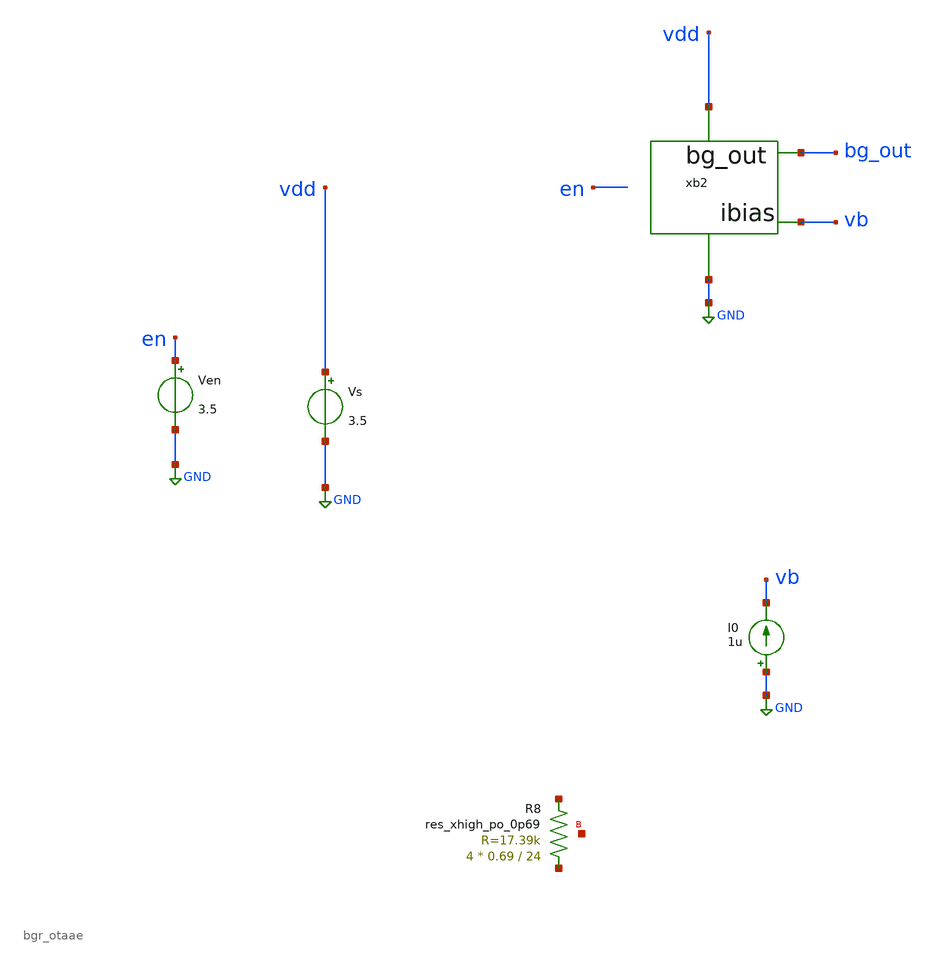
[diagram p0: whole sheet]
** sch_path: bg_sim_jm_otaam.sch
**.subckt bg_sim_jm_otaam
Vs vdd GND 3.5
Ven en GND 3.5
XR8 net1 net2 net3 sky130_fd_pr__res_xhigh_po_0p69 L=24 mult=4 m=4
I0 GND vb 1u
xb2 bg_out vb GND vdd bgr_otaae
**** begin user architecture code



.options method=gear
*.options method=trap
.options maxorder=3
.param R=36k
.save all
*R10 ldo_out GND {R}
*IL ldo_out 0 PWL(0 0.1m 10u 0.1m 20u 10m 30u 10m)
*CL ldo_out gnd 10p
*.lib /home/mustafa/mabrains/pdks/share/pdk/sky130A/libs.tech/ngspice/sky130.lib_mod.spice tt
.lib /foss/pdks/sky130A/libs.tech/ngspice/sky130.lib.spice TT





.nodeset v(x1.inn)=1.2
.nodeset v(x1.inp)=1.2
.nodeset v(x1.mir)=1
.nodeset v(x1.net5)=1
.nodeset v(x1.bg_out)=1.1
*.nodeset v(ldo_out)=1.8
*.nodeset v(pos)=1.1
*.nodeset v(net3)=0.8
*.nodeset v(net1)=0.7
.nodeset v(x1.net6)=0.9
*.nodeset v(net7)=0.75
.nodeset v(xy1.vb)=0.9


.option temp=27
*User_defined_functions
.control
define max(vector_name) (vecmax(vector_name))
define min(vector_name) (vecmin(vector_name))
.endc


*Temp_sweep
.control
*alter IL 0
dc temp 85 0 -1
let temp_coeff=1000000*(max(bg_out)-min(bg_out))/85
print temp_coeff
*plot v(ldo_out)
plot v(bg_out)
plot i(vs)
set wr_singlescale
set wr_vecnames
set appendwrite
.endc


.control
*alter IL 0
*alter R10 1G
op
let iq =i(Vs)
print iq
*print all
set wr_singlescale
set wr_vecnames
set appendwrite
*if v(ldo_out)>1
*wrdata op_point_test v(ldo_out)
*end
.endc


*PSRR_Analysis
.control
*alter IL 0
alter Vs AC =1
*alter Vt AC=0
*alter L1 0
*alter C2 0
ac dec 10 1 1G
meas AC PSRR100 FIND vdb(bg_out) AT=100
meas AC PSRR100k FIND vdb(bg_out) AT=100k
*plot vdb(ldo_out)
plot vdb(bg_out)
.endc



**** end user architecture code
**.ends
.GLOBAL GND
.end
